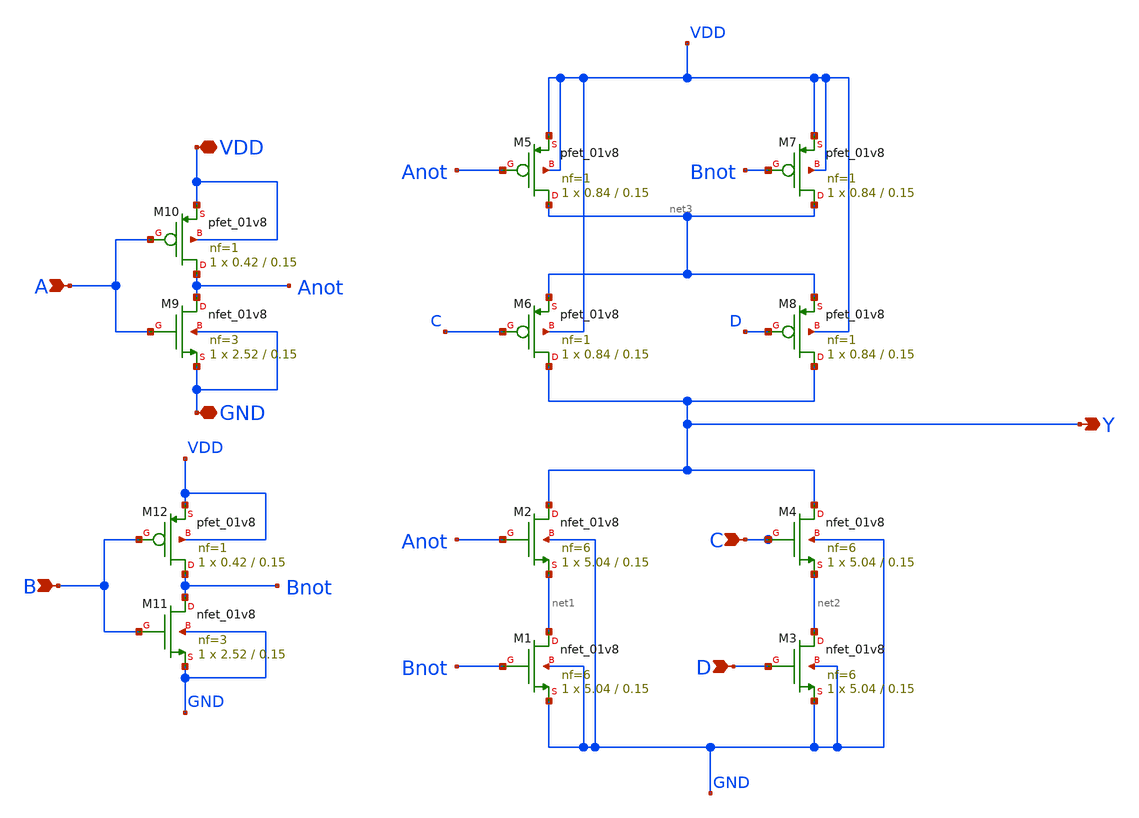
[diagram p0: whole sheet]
** sch_path: cells/MAOI4X1/schematic/maoi4x1.sch
**.subckt maoi4x1 A VDD GND B Y D C
*.ipin A
*.iopin VDD
*.iopin GND
*.ipin B
*.opin Y
*.ipin D
*.ipin C
XM9 Anot A GND GND sky130_fd_pr__nfet_01v8 L=0.15 W=2.52 nf=3 ad='int((3 + 1)/2) * 2.52 / 3 * 0.29' as='int((3 + 2)/2) * 2.52 / 3 * 0.29'
+ pd='2*int((3 + 1)/2) * (2.52 / 3 + 0.29)' ps='2*int((3 + 2)/2) * (2.52 / 3 + 0.29)' nrd='0.29 / 2.52 '
+ nrs='0.29 / 2.52 ' sa=0 sb=0 sd=0 mult=1 m=1
XM2 Y Anot net1 GND sky130_fd_pr__nfet_01v8 L=0.15 W=5.04 nf=6 ad='int((6 + 1)/2) * 5.04 / 6 * 0.29'
+ as='int((6 + 2)/2) * 5.04 / 6 * 0.29' pd='2*int((6 + 1)/2) * (5.04 / 6 + 0.29)' ps='2*int((6 + 2)/2) * (5.04 / 6 + 0.29)'
+ nrd='0.29 / 5.04 ' nrs='0.29 / 5.04 ' sa=0 sb=0 sd=0 mult=1 m=1
XM5 net3 Anot VDD VDD sky130_fd_pr__pfet_01v8 L=0.15 W=0.84 nf=1 ad='int((1 + 1)/2) * 0.84 / 1 * 0.29'
+ as='int((1 + 2)/2) * 0.84 / 1 * 0.29' pd='2*int((1 + 1)/2) * (0.84 / 1 + 0.29)' ps='2*int((1 + 2)/2) * (0.84 / 1 + 0.29)'
+ nrd='0.29 / 0.84 ' nrs='0.29 / 0.84 ' sa=0 sb=0 sd=0 mult=1 m=1
XM10 Anot A VDD VDD sky130_fd_pr__pfet_01v8 L=0.15 W=0.42 nf=1 ad='int((1 + 1)/2) * 0.42 / 1 * 0.29'
+ as='int((1 + 2)/2) * 0.42 / 1 * 0.29' pd='2*int((1 + 1)/2) * (0.42 / 1 + 0.29)' ps='2*int((1 + 2)/2) * (0.42 / 1 + 0.29)'
+ nrd='0.29 / 0.42 ' nrs='0.29 / 0.42 ' sa=0 sb=0 sd=0 mult=1 m=1
XM7 net3 Bnot VDD VDD sky130_fd_pr__pfet_01v8 L=0.15 W=0.84 nf=1 ad='int((1 + 1)/2) * 0.84 / 1 * 0.29'
+ as='int((1 + 2)/2) * 0.84 / 1 * 0.29' pd='2*int((1 + 1)/2) * (0.84 / 1 + 0.29)' ps='2*int((1 + 2)/2) * (0.84 / 1 + 0.29)'
+ nrd='0.29 / 0.84 ' nrs='0.29 / 0.84 ' sa=0 sb=0 sd=0 mult=1 m=1
XM8 Y D net3 VDD sky130_fd_pr__pfet_01v8 L=0.15 W=0.84 nf=1 ad='int((1 + 1)/2) * 0.84 / 1 * 0.29' as='int((1 + 2)/2) * 0.84 / 1 * 0.29'
+ pd='2*int((1 + 1)/2) * (0.84 / 1 + 0.29)' ps='2*int((1 + 2)/2) * (0.84 / 1 + 0.29)' nrd='0.29 / 0.84 '
+ nrs='0.29 / 0.84 ' sa=0 sb=0 sd=0 mult=1 m=1
XM6 Y C net3 VDD sky130_fd_pr__pfet_01v8 L=0.15 W=0.84 nf=1 ad='int((1 + 1)/2) * 0.84 / 1 * 0.29' as='int((1 + 2)/2) * 0.84 / 1 * 0.29'
+ pd='2*int((1 + 1)/2) * (0.84 / 1 + 0.29)' ps='2*int((1 + 2)/2) * (0.84 / 1 + 0.29)' nrd='0.29 / 0.84 '
+ nrs='0.29 / 0.84 ' sa=0 sb=0 sd=0 mult=1 m=1
XM4 Y C net2 GND sky130_fd_pr__nfet_01v8 L=0.15 W=5.04 nf=6 ad='int((6 + 1)/2) * 5.04 / 6 * 0.29' as='int((6 + 2)/2) * 5.04 / 6 * 0.29'
+ pd='2*int((6 + 1)/2) * (5.04 / 6 + 0.29)' ps='2*int((6 + 2)/2) * (5.04 / 6 + 0.29)' nrd='0.29 / 5.04 '
+ nrs='0.29 / 5.04 ' sa=0 sb=0 sd=0 mult=1 m=1
XM3 net2 D GND GND sky130_fd_pr__nfet_01v8 L=0.15 W=5.04 nf=6 ad='int((6 + 1)/2) * 5.04 / 6 * 0.29' as='int((6 + 2)/2) * 5.04 / 6 * 0.29'
+ pd='2*int((6 + 1)/2) * (5.04 / 6 + 0.29)' ps='2*int((6 + 2)/2) * (5.04 / 6 + 0.29)' nrd='0.29 / 5.04 '
+ nrs='0.29 / 5.04 ' sa=0 sb=0 sd=0 mult=1 m=1
XM1 net1 Bnot GND GND sky130_fd_pr__nfet_01v8 L=0.15 W=5.04 nf=6 ad='int((6 + 1)/2) * 5.04 / 6 * 0.29'
+ as='int((6 + 2)/2) * 5.04 / 6 * 0.29' pd='2*int((6 + 1)/2) * (5.04 / 6 + 0.29)' ps='2*int((6 + 2)/2) * (5.04 / 6 + 0.29)'
+ nrd='0.29 / 5.04 ' nrs='0.29 / 5.04 ' sa=0 sb=0 sd=0 mult=1 m=1
XM11 Bnot B GND GND sky130_fd_pr__nfet_01v8 L=0.15 W=2.52 nf=3 ad='int((3 + 1)/2) * 2.52 / 3 * 0.29'
+ as='int((3 + 2)/2) * 2.52 / 3 * 0.29' pd='2*int((3 + 1)/2) * (2.52 / 3 + 0.29)' ps='2*int((3 + 2)/2) * (2.52 / 3 + 0.29)'
+ nrd='0.29 / 2.52 ' nrs='0.29 / 2.52 ' sa=0 sb=0 sd=0 mult=1 m=1
XM12 Bnot B VDD VDD sky130_fd_pr__pfet_01v8 L=0.15 W=0.42 nf=1 ad='int((1 + 1)/2) * 0.42 / 1 * 0.29'
+ as='int((1 + 2)/2) * 0.42 / 1 * 0.29' pd='2*int((1 + 1)/2) * (0.42 / 1 + 0.29)' ps='2*int((1 + 2)/2) * (0.42 / 1 + 0.29)'
+ nrd='0.29 / 0.42 ' nrs='0.29 / 0.42 ' sa=0 sb=0 sd=0 mult=1 m=1
**.ends
.end
